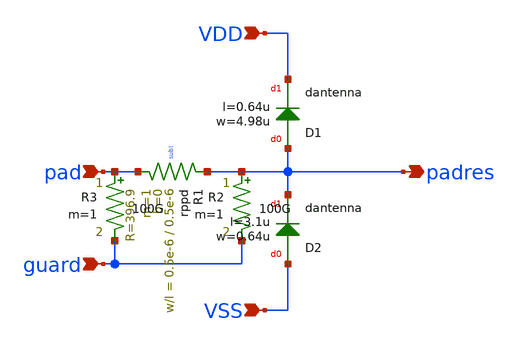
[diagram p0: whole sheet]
** sch_path: trident_test_structures/design_data/xschem/IOPadAnalog_submodules/sg13g2_SecondaryProtection.sch
**.subckt sg13g2_SecondaryProtection pad VDD VSS padres guard
*.ipin pad
*.ipin VDD
*.ipin VSS
*.opin padres
*.ipin guard
XR1 padres pad sub! rppd w=0.5e-6 l=0.5e-6 m=1 b=0 mm_ok=1
XD1 padres VDD dantenna l=0.64u w=4.98u
XD2 VSS padres dantenna l=3.1u w=0.64u
R2 padres guard 100G m=1
R3 pad guard 100G m=1
**.ends
.end
